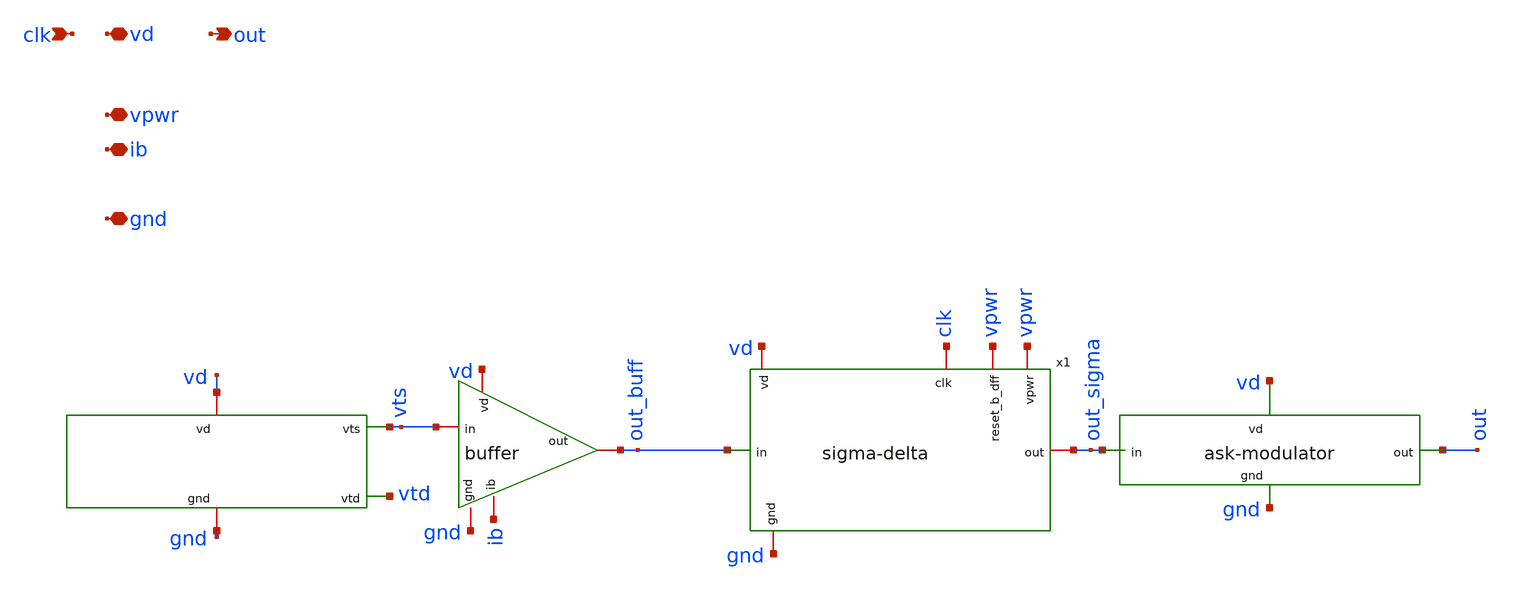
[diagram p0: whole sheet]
** sch_path: device-complete/xschem/device-complete.sch
**.subckt device-complete vd clk out vpwr ib gnd
*.iopin vd
*.ipin clk
*.opin out
*.iopin vpwr
*.iopin ib
*.iopin gnd
x3 vd vts vtd gnd sensor
X2 vd vts out_buff ib gnd buffer
x1 vpwr clk out_sigma out_buff vpwr gnd vd sigma-delta
x4 vd out out_sigma gnd ask-modulator
**.ends
.end
